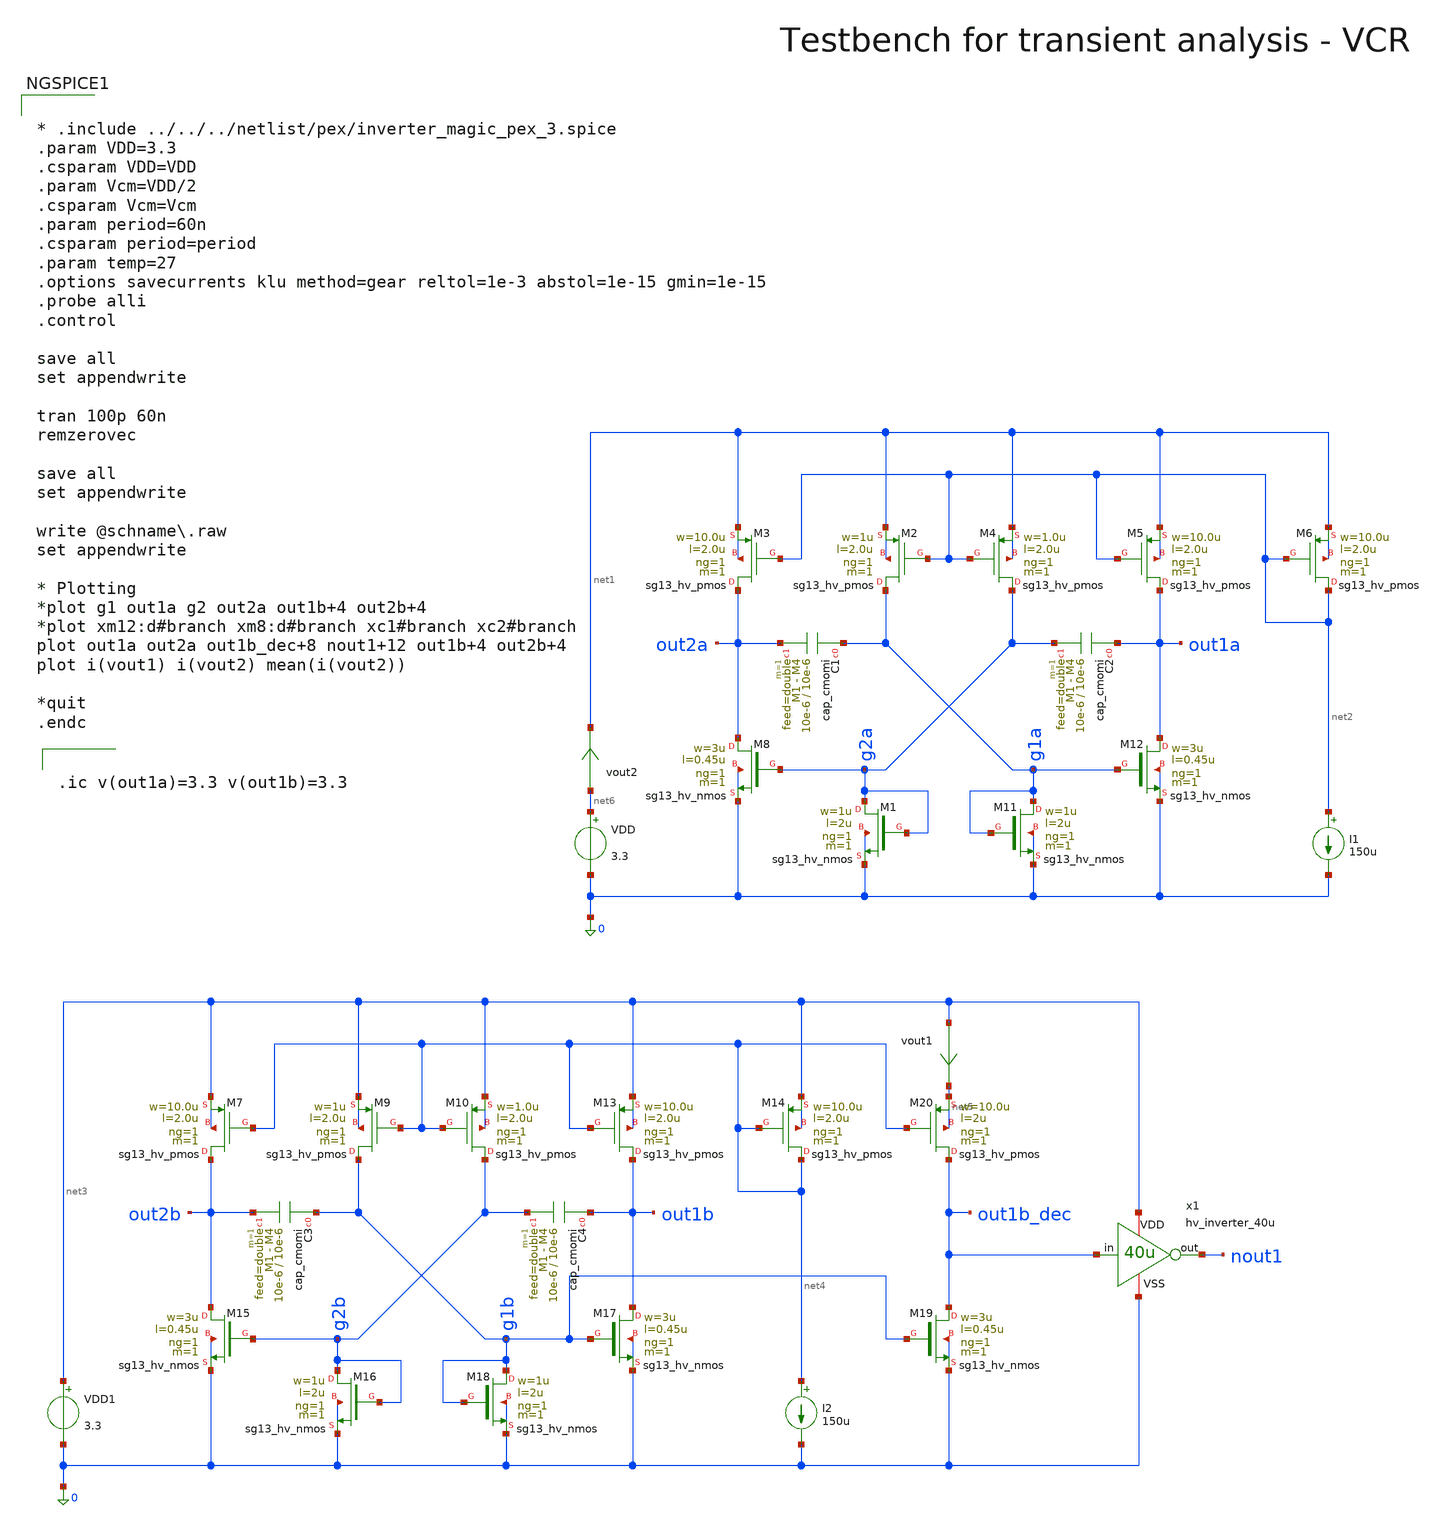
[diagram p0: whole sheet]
** sch_path: macros/heichips26_vcr/macros/switched_capacitor/testbenches/xschem/osc_tb_tran.sch
**.subckt osc_tb_tran
VDD net6 0 3.3
I1 net2 0 150u
XM3 out2a net2 net1 net1 sg13_hv_pmos w=10.0u l=2.0u ng=1 m=1 mm_ok=1
XM2 g1a net2 net1 net1 sg13_hv_pmos w=1u l=2.0u ng=1 m=1 mm_ok=1
XM4 g2a net2 net1 net1 sg13_hv_pmos w=1.0u l=2.0u ng=1 m=1 mm_ok=1
XM5 out1a net2 net1 net1 sg13_hv_pmos w=10.0u l=2.0u ng=1 m=1 mm_ok=1
XM6 net2 net2 net1 net1 sg13_hv_pmos w=10.0u l=2.0u ng=1 m=1 mm_ok=1
XC1 g1a out2a cap_cmomi w=10e-6 l=10e-6 mmin=1 mmax=4 feed=double subblock=0 m=1 mm_ok=1
XC2 out1a g2a cap_cmomi w=10e-6 l=10e-6 mmin=1 mmax=4 feed=double subblock=0 m=1 mm_ok=1
XM8 out2a g2a 0 0 sg13_hv_nmos w=3u l=0.45u ng=1 m=1 mm_ok=1
XM1 g2a g2a 0 0 sg13_hv_nmos w=1u l=2u ng=1 m=1 mm_ok=1
XM12 out1a g1a 0 0 sg13_hv_nmos w=3u l=0.45u ng=1 m=1 mm_ok=1
XM11 g1a g1a 0 0 sg13_hv_nmos w=1u l=2u ng=1 m=1 mm_ok=1
VDD1 net3 0 3.3
I2 net4 0 150u
XM7 out2b net4 net3 net3 sg13_hv_pmos w=10.0u l=2.0u ng=1 m=1 mm_ok=1
XM9 g1b net4 net3 net3 sg13_hv_pmos w=1u l=2.0u ng=1 m=1 mm_ok=1
XM10 g2b net4 net3 net3 sg13_hv_pmos w=1.0u l=2.0u ng=1 m=1 mm_ok=1
XM13 out1b net4 net3 net3 sg13_hv_pmos w=10.0u l=2.0u ng=1 m=1 mm_ok=1
XM14 net4 net4 net3 net3 sg13_hv_pmos w=10.0u l=2.0u ng=1 m=1 mm_ok=1
XC3 g1b out2b cap_cmomi w=10e-6 l=10e-6 mmin=1 mmax=4 feed=double subblock=0 m=1 mm_ok=1
XC4 out1b g2b cap_cmomi w=10e-6 l=10e-6 mmin=1 mmax=4 feed=double subblock=0 m=1 mm_ok=1
XM15 out2b g2b 0 0 sg13_hv_nmos w=3u l=0.45u ng=1 m=1 mm_ok=1
XM16 g2b g2b 0 0 sg13_hv_nmos w=1u l=2u ng=1 m=1 mm_ok=1
XM17 out1b g1b 0 0 sg13_hv_nmos w=3u l=0.45u ng=1 m=1 mm_ok=1
XM18 g1b g1b 0 0 sg13_hv_nmos w=1u l=2u ng=1 m=1 mm_ok=1
x1 net3 out1b_dec nout1 0 hv_inverter_40u
XM19 out1b_dec g1b 0 0 sg13_hv_nmos w=3u l=0.45u ng=1 m=1 mm_ok=1
XM20 out1b_dec net4 net5 net5 sg13_hv_pmos w=10.0u l=2u ng=1 m=1 mm_ok=1
vout1 net3 net5 0
.save i(vout1)
vout2 net6 net1 0
.save i(vout2)
**** begin user architecture code

.lib cornerMOSlv.lib mos_tt
.lib cornerMOShv.lib mos_tt
.lib cornerRES.lib res_typ
.lib cornerDIO.lib dio_tt
.lib cornerCAP.lib cap_typ

.include $::PDK_ROOT/$::PDK/libs.ref/sg13cmos5l_stdcell/spice/sg13cmos5l_stdcell.spice



* .include ../../../netlist/pex/inverter_magic_pex_3.spice
.param VDD=3.3
.csparam VDD=VDD
.param Vcm=VDD/2
.csparam Vcm=Vcm
.param period=60n
.csparam period=period
.param temp=27
.options savecurrents klu method=gear reltol=1e-3 abstol=1e-15 gmin=1e-15
.probe alli
.control

save all
set appendwrite

tran 100p 60n
remzerovec

save all
set appendwrite

write @schname\.raw
set appendwrite

* Plotting
*plot g1 out1a g2 out2a out1b+4 out2b+4
*plot xm12:d#branch xm8:d#branch xc1#branch xc2#branch
plot out1a out2a out1b_dec+8 nout1+12 out1b+4 out2b+4
plot i(vout1) i(vout2) mean(i(vout2))

*quit
.endc




.ic v(out1a)=3.3 v(out1b)=3.3


**** end user architecture code
**.ends

* expanding   symbol:  hv_inverter_40u.sym # of pins=4
** sym_path: macros/heichips26_vcr/macros/switched_capacitor/schematic/xschem/hv_inverter_40u.sym
** sch_path: macros/heichips26_vcr/macros/switched_capacitor/schematic/xschem/hv_inverter_40u.sch
.subckt hv_inverter_40u VDD in out VSS
*.ipin in
*.iopin VDD
*.iopin VSS
*.opin out
XM2 out in VSS VSS sg13_hv_nmos w={n_w} l={n_l} ng={ng} m=1 mm_ok=1
XM3 out in VDD VDD sg13_hv_pmos w={p_w} l={p_l} ng={ng} m=1 mm_ok=1
**** begin user architecture code


.param w   = 10u
.param ng  = 4
.param n_ng = ng
.param n_w = {3u*n_ng}
.param n_l = 0.45u
.param p_ng = ng
.param p_w = {10u*p_ng}
.param p_l = 0.4u


**** end user architecture code
.ends

.end
